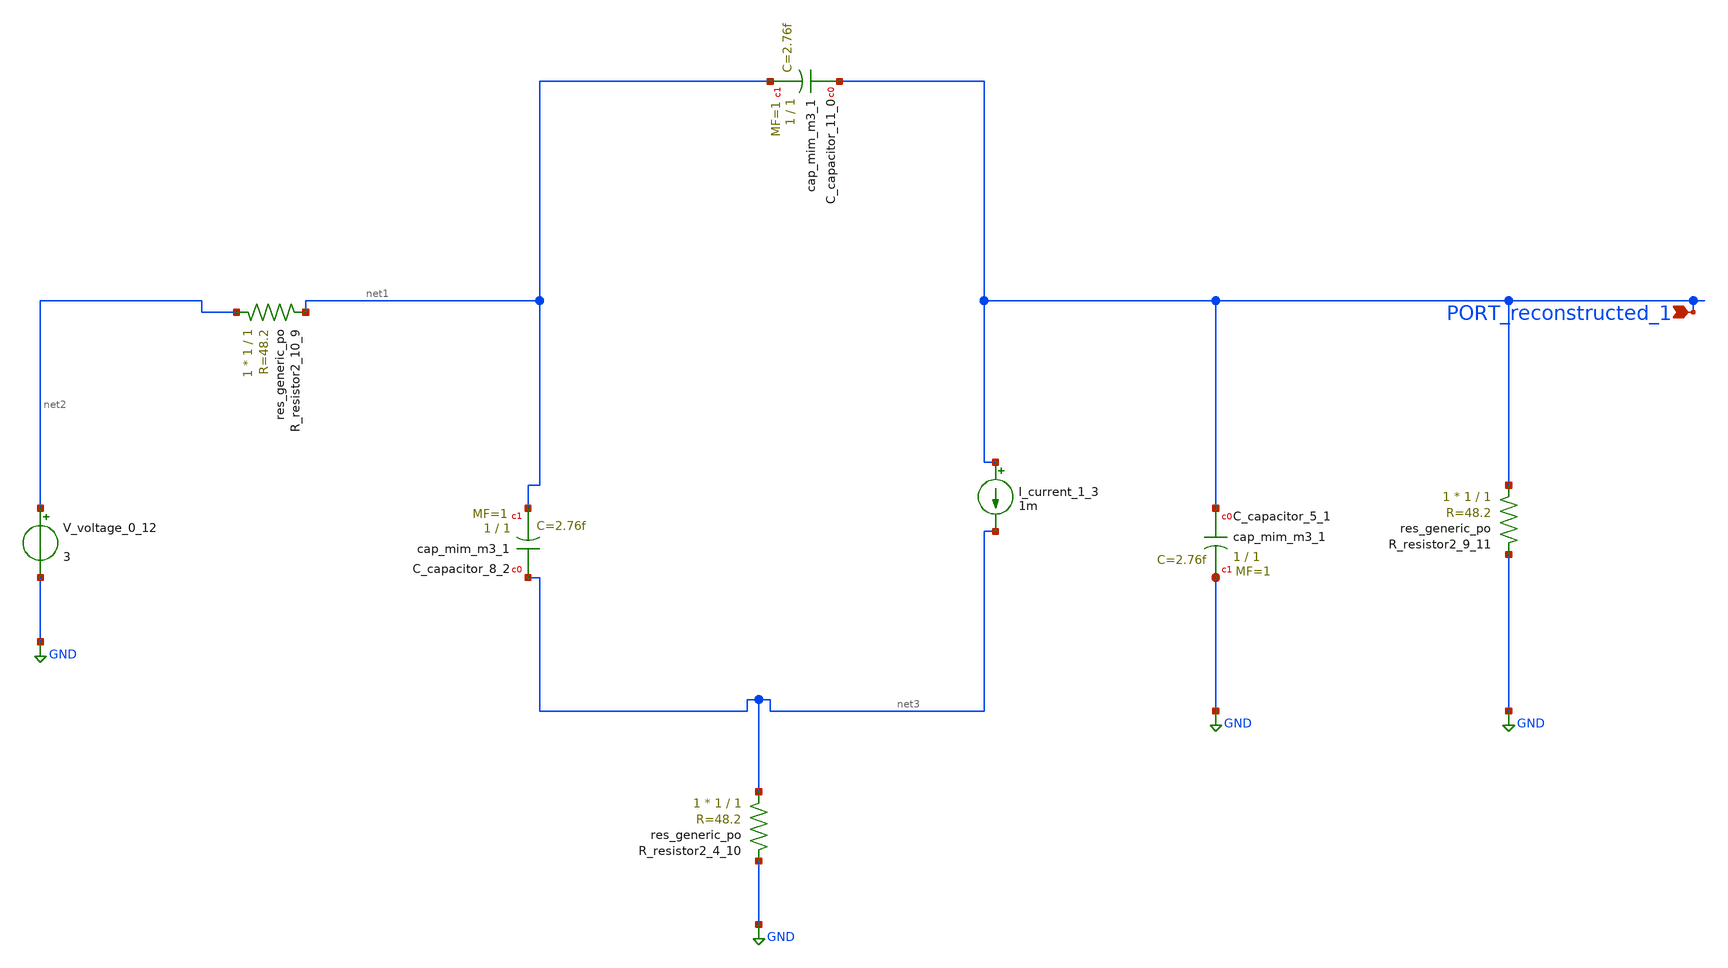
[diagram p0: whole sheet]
** sch_path: schematics/AMSNet/404.sch
**.subckt 404 PORT_reconstructed_1
*.ipin PORT_reconstructed_1
XC_capacitor_11_0 PORT_reconstructed_1 net1 sky130_fd_pr__cap_mim_m3_1 W=1 L=1 MF=1 m=1
XC_capacitor_5_1 PORT_reconstructed_1 GND sky130_fd_pr__cap_mim_m3_1 W=1 L=1 MF=1 m=1
XC_capacitor_8_2 net3 net1 sky130_fd_pr__cap_mim_m3_1 W=1 L=1 MF=1 m=1
I_current_1_3 PORT_reconstructed_1 net3 1m
XR_resistor2_10_9 net2 net1 sky130_fd_pr__res_generic_po W=1 L=1 m=1
XR_resistor2_4_10 net3 GND sky130_fd_pr__res_generic_po W=1 L=1 m=1
XR_resistor2_9_11 PORT_reconstructed_1 GND sky130_fd_pr__res_generic_po W=1 L=1 m=1
V_voltage_0_12 net2 GND 3
**.ends
.GLOBAL GND
.end
